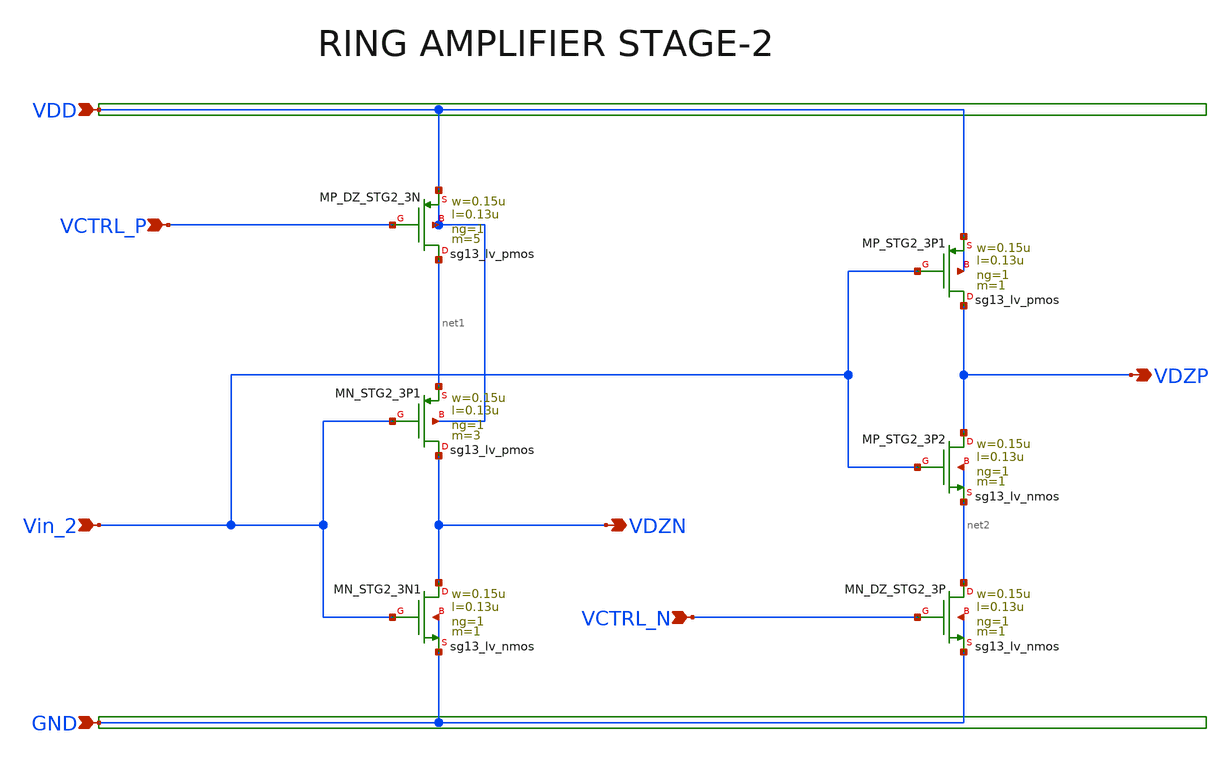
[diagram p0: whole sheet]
** sch_path: Design Files/RAMP/Fully-Diff-RAMP/STG2.sch
**.subckt STG2 Vin_2 VDD GND VCTRL_P VCTRL_N VDZN VDZP
*.ipin Vin_2
*.ipin VDD
*.ipin GND
*.ipin VCTRL_P
*.ipin VCTRL_N
*.opin VDZN
*.opin VDZP
XMN_STG2_3N1 VDZN Vin_2 GND GND sg13_lv_nmos w=0.15u l=0.13u ng=1 m=1 mm_ok=1
XMN_STG2_3P1 VDZN Vin_2 net1 VDD sg13_lv_pmos w=0.15u l=0.13u ng=1 m=3 mm_ok=1
XMP_DZ_STG2_3N net1 VCTRL_P VDD VDD sg13_lv_pmos w=0.15u l=0.13u ng=1 m=5 mm_ok=1
XMP_STG2_3P2 VDZP Vin_2 net2 net2 sg13_lv_nmos w=0.15u l=0.13u ng=1 m=1 mm_ok=1
XMP_STG2_3P1 VDZP Vin_2 VDD VDD sg13_lv_pmos w=0.15u l=0.13u ng=1 m=1 mm_ok=1
XMN_DZ_STG2_3P net2 VCTRL_N GND GND sg13_lv_nmos w=0.15u l=0.13u ng=1 m=1 mm_ok=1
**.ends
.end
